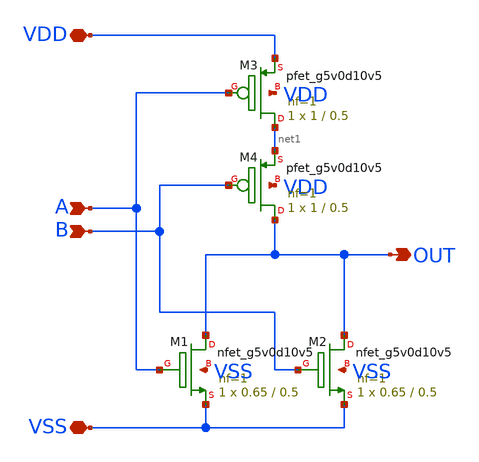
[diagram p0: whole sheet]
** sch_path: xschem/nor2.sch
**.subckt nor2 VSS VDD B A OUT
*.iopin VSS
*.iopin VDD
*.ipin B
*.ipin A
*.opin OUT
XM2 OUT B VSS VSS sky130_fd_pr__nfet_g5v0d10v5 L=0.5 W=0.65 nf=1 ad='int((1 + 1)/2) * 0.65 / 1 * 0.29'
+ as='int((1 + 2)/2) * 0.65 / 1 * 0.29' pd='2*int((1 + 1)/2) * (0.65 / 1 + 0.29)' ps='2*int((1 + 2)/2) * (0.65 / 1 + 0.29)'
+ nrd='0.29 / 0.65 ' nrs='0.29 / 0.65 ' sa=0 sb=0 sd=0 mult=1 m=1
XM1 OUT A VSS VSS sky130_fd_pr__nfet_g5v0d10v5 L=0.5 W=0.65 nf=1 ad='int((1 + 1)/2) * 0.65 / 1 * 0.29'
+ as='int((1 + 2)/2) * 0.65 / 1 * 0.29' pd='2*int((1 + 1)/2) * (0.65 / 1 + 0.29)' ps='2*int((1 + 2)/2) * (0.65 / 1 + 0.29)'
+ nrd='0.29 / 0.65 ' nrs='0.29 / 0.65 ' sa=0 sb=0 sd=0 mult=1 m=1
XM3 net1 A VDD VDD sky130_fd_pr__pfet_g5v0d10v5 L=0.5 W=1 nf=1 ad='int((1 + 1)/2) * 1 / 1 * 0.29' as='int((1 + 2)/2) * 1 / 1 * 0.29'
+ pd='2*int((1 + 1)/2) * (1 / 1 + 0.29)' ps='2*int((1 + 2)/2) * (1 / 1 + 0.29)' nrd='0.29 / 1 ' nrs='0.29 / 1 '
+ sa=0 sb=0 sd=0 mult=1 m=1
XM4 OUT B net1 VDD sky130_fd_pr__pfet_g5v0d10v5 L=0.5 W=1 nf=1 ad='int((1 + 1)/2) * 1 / 1 * 0.29' as='int((1 + 2)/2) * 1 / 1 * 0.29'
+ pd='2*int((1 + 1)/2) * (1 / 1 + 0.29)' ps='2*int((1 + 2)/2) * (1 / 1 + 0.29)' nrd='0.29 / 1 ' nrs='0.29 / 1 '
+ sa=0 sb=0 sd=0 mult=1 m=1
**.ends
.end
